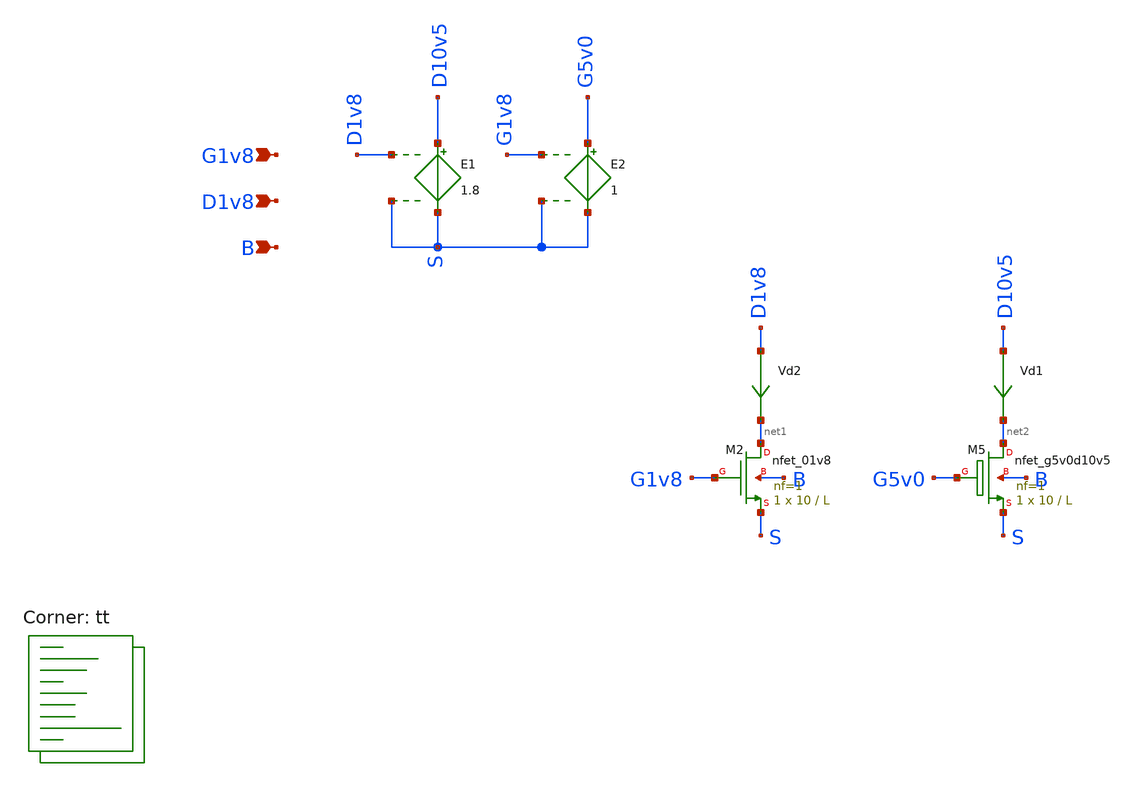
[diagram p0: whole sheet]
** sch_path: userLib/userLib/NmosTest.sch
**.subckt NmosTest G1v8 D1v8 B
*.ipin G1v8
*.ipin D1v8
*.ipin B
Vd2 D1v8 net1 0
.save i(vd2)
Vd1 D10v5 net2 0
.save i(vd1)
XM2 net1 G1v8 S B sky130_fd_pr__nfet_01v8 L=L W=10 nf=1 ad='int((1 + 1)/2) * 10 / 1 * 0.29' as='int((1 + 2)/2) * 10 / 1 * 0.29'
+ pd='2*int((1 + 1)/2) * (10 / 1 + 0.29)' ps='2*int((1 + 2)/2) * (10 / 1 + 0.29)' nrd='0.29 / 10 ' nrs='0.29 / 10 '
+ sa=0 sb=0 sd=0 mult=1 m=1
XM5 net2 G5v0 S B sky130_fd_pr__nfet_g5v0d10v5 L=L W=10 nf=1 ad='int((1 + 1)/2) * 10 / 1 * 0.29' as='int((1 + 2)/2) * 10 / 1 * 0.29'
+ pd='2*int((1 + 1)/2) * (10 / 1 + 0.29)' ps='2*int((1 + 2)/2) * (10 / 1 + 0.29)' nrd='0.29 / 10 ' nrs='0.29 / 10 '
+ sa=0 sb=0 sd=0 mult=1 m=1
E1 D10v5 S D1v8 S 1.8
E2 G5v0 S G1v8 S 1
**** begin user architecture code

* this option enables mos model bin
* selection based on W/NF instead of W
.option wnflag=1
.option savecurrents
.param L = 0.5
V1 D1v8 0 0
V2 G1v8 0 0.75
vs s 0 0
vb b 0 0
.control
save all

save @m.xm5.msky130_fd_pr__nfet_g5v0d10v5[gm]
save @m.xm5.msky130_fd_pr__nfet_g5v0d10v5[vth]
save @m.xm5.msky130_fd_pr__nfet_g5v0d10v5[gds]
save @m.xm5.msky130_fd_pr__nfet_g5v0d10v5[cgg]
save @m.xm5.msky130_fd_pr__nfet_g5v0d10v5[vgs]
save @m.xm2.msky130_fd_pr__nfet_01v8[gm]
save @m.xm2.msky130_fd_pr__nfet_01v8[vth]
save @m.xm2.msky130_fd_pr__nfet_01v8[gds]
save @m.xm2.msky130_fd_pr__nfet_01v8[cgg]
save @m.xm2.msky130_fd_pr__nfet_01v8[vgs]
let l_max = 1
let l_start = 1
let l_delta = 1
let l_actual = l_start

while l_actual le l_max
 alter L l_actual

 dc V1 0 1.8 0.01
 write test_nmos.raw

 let l_actual = l_actual + l_delta

end

plot all.vd1#branch vs D10v5
plot all.vd2#branch vs D1v8
plot all.@m.xm5.msky130_fd_pr__nfet_g5v0d10v5[gm] vs all.vd1#branch
plot all.@m.xm2.msky130_fd_pr__nfet_01v8[gm] vs all.vd2#branch
set appendwrite
op
set filetype=binary
write test_nmos.raw

set wr_singlescale
set wr_vecnames
wrdata nmosTparams.txt  dc2.i(vd2) dc2.v(D10v5) dc2.v(G5v0)
+ dc2.@m.xm5.msky130_fd_pr__nfet_g5v0d10v5[gm] dc2.@m.xm5.msky130_fd_pr__nfet_g5v0d10v5[vth] dc2.@m.xm5.msky130_fd_pr__nfet_g5v0d10v5[gds]
+ dc2.@m.xm5.msky130_fd_pr__nfet_g5v0d10v5[cgg] dc2.@m.xm5.msky130_fd_pr__nfet_g5v0d10v5[vgs] dc2.@m.xm2.msky130_fd_pr__nfet_01v8[gm]
+ dc2.@m.xm2.msky130_fd_pr__nfet_01v8[vth] dc2.@m.xm2.msky130_fd_pr__nfet_01v8[gds] dc2.@m.xm2.msky130_fd_pr__nfet_01v8[cgg]
+ dc2.@m.xm2.msky130_fd_pr__nfet_01v8[vgs]
.endc


.lib $::SKYWATER_MODELS/sky130.lib.spice tt
**** end user architecture code
**.ends
.end
